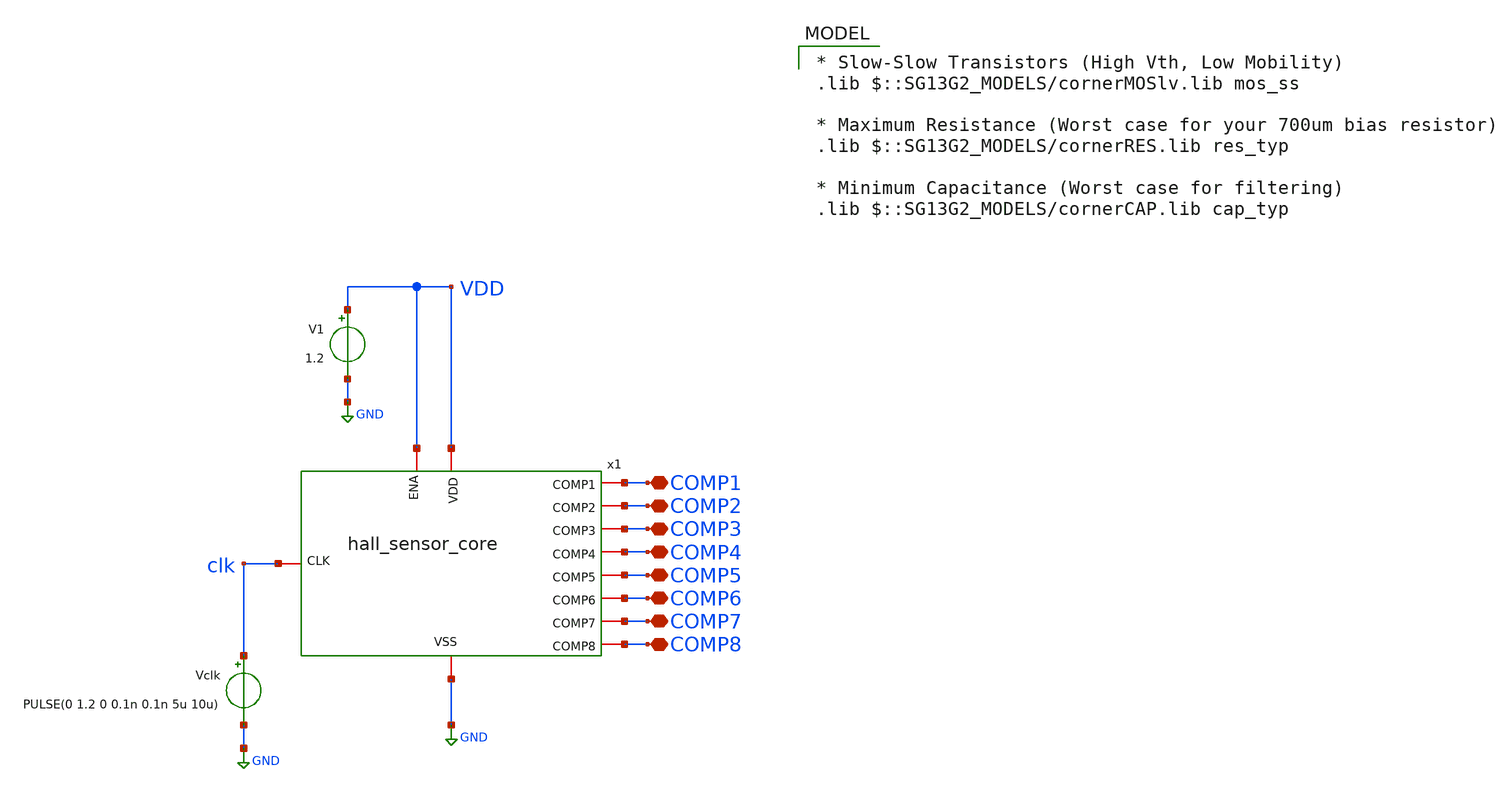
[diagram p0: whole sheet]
** sch_path: xschem/Hall_Core_TB.sch
**.subckt Hall_Core_TB COMP2 COMP3 COMP4 COMP5 COMP6 COMP7 COMP8 COMP1
*.iopin COMP2
*.iopin COMP3
*.iopin COMP4
*.iopin COMP5
*.iopin COMP6
*.iopin COMP7
*.iopin COMP8
*.iopin COMP1
x1 COMP1 COMP2 COMP3 COMP4 COMP5 COMP6 COMP7 GND VDD COMP8 clk VDD hall_sensor_core
V1 VDD GND 1.2
Vclk clk GND PULSE(0 1.2 0 0.1n 0.1n 5u 10u)
**** begin user architecture code
 * Slow-Slow Transistors (High Vth, Low Mobility)
.lib $::SG13G2_MODELS/cornerMOSlv.lib mos_ss

* Maximum Resistance (Worst case for your 700um bias resistor)
.lib $::SG13G2_MODELS/cornerRES.lib res_typ

* Minimum Capacitance (Worst case for filtering)
.lib $::SG13G2_MODELS/cornerCAP.lib cap_typ

.control
  save all

  * ==========================================
  * HYSTERESIS SWEEP: 10ms
  * ==========================================
  * Route through X1 (Core) down to X_HALL (Hall block)
  alter @r.x1.x1.r1[resistance] = 1000
  alter @r.x1.x1.r2[resistance] = 1000
  alter @r.x1.x1.r3[resistance] = 1000
  alter @r.x1.x1.r4[resistance] = 1000

  * Route the PWL voltage sweep directly into the 2nd layer
  alter @v.x1.x1.vb[pwl] = [ 0 0 5m 0.1905 10m 0 ]

  * (Keep your MAGIC SAUCE options here)
  .options itl4=100 reltol=0.01 method=gear cshunt=10f

  tran 100n 10m

  plot v(x1.amp_out) v(comp1) v(comp2) v(comp3) v(comp4) v(comp5) v(comp6) v(comp7) v(comp8) title 'Hysteresis_and_Comparators'
.endc

**** end user architecture code
**.ends
.GLOBAL GND
.end
